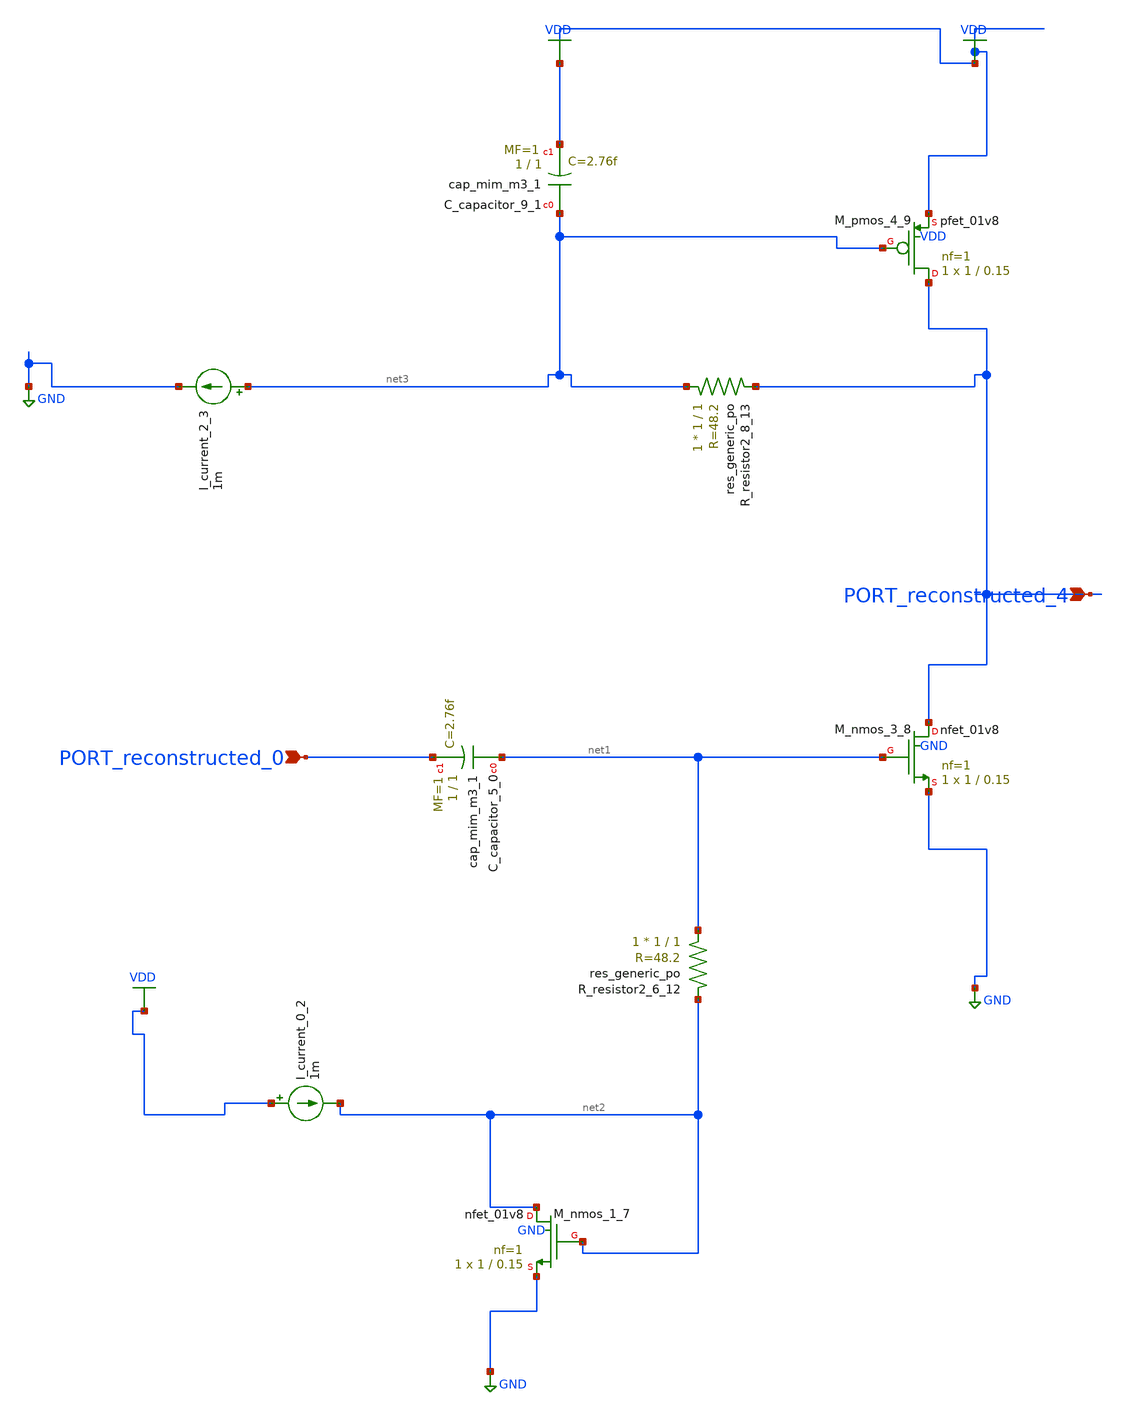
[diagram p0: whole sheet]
** sch_path: schematics/AMSNet/307.sch
**.subckt 307 PORT_reconstructed_4 PORT_reconstructed_0
*.ipin PORT_reconstructed_4
*.ipin PORT_reconstructed_0
XC_capacitor_5_0 net1 PORT_reconstructed_0 sky130_fd_pr__cap_mim_m3_1 W=1 L=1 MF=1 m=1
XC_capacitor_9_1 net3 VDD sky130_fd_pr__cap_mim_m3_1 W=1 L=1 MF=1 m=1
I_current_0_2 VDD net2 1m
I_current_2_3 net3 GND 1m
XM_nmos_1_7 net2 net2 GND GND sky130_fd_pr__nfet_01v8 L=0.15 W=1 nf=1 ad='int((1 + 1)/2) * 1 / 1 * 0.29'
+ as='int((1 + 2)/2) * 1 / 1 * 0.29' pd='2*int((1 + 1)/2) * (1 / 1 + 0.29)' ps='2*int((1 + 2)/2) * (1 / 1 + 0.29)'
+ nrd='0.29 / 1 ' nrs='0.29 / 1 ' sa=0 sb=0 sd=0 mult=1 m=1
XM_nmos_3_8 PORT_reconstructed_4 net1 GND GND sky130_fd_pr__nfet_01v8 L=0.15 W=1 nf=1 ad='int((1 + 1)/2) * 1 / 1 * 0.29'
+ as='int((1 + 2)/2) * 1 / 1 * 0.29' pd='2*int((1 + 1)/2) * (1 / 1 + 0.29)' ps='2*int((1 + 2)/2) * (1 / 1 + 0.29)'
+ nrd='0.29 / 1 ' nrs='0.29 / 1 ' sa=0 sb=0 sd=0 mult=1 m=1
XM_pmos_4_9 PORT_reconstructed_4 net3 VDD VDD sky130_fd_pr__pfet_01v8 L=0.15 W=1 nf=1 ad='int((1 + 1)/2) * 1 / 1 * 0.29'
+ as='int((1 + 2)/2) * 1 / 1 * 0.29' pd='2*int((1 + 1)/2) * (1 / 1 + 0.29)' ps='2*int((1 + 2)/2) * (1 / 1 + 0.29)'
+ nrd='0.29 / 1 ' nrs='0.29 / 1 ' sa=0 sb=0 sd=0 mult=1 m=1
XR_resistor2_6_12 net1 net2 sky130_fd_pr__res_generic_po W=1 L=1 m=1
XR_resistor2_8_13 net3 PORT_reconstructed_4 sky130_fd_pr__res_generic_po W=1 L=1 m=1
**.ends
.GLOBAL GND
.GLOBAL VDD
.end
